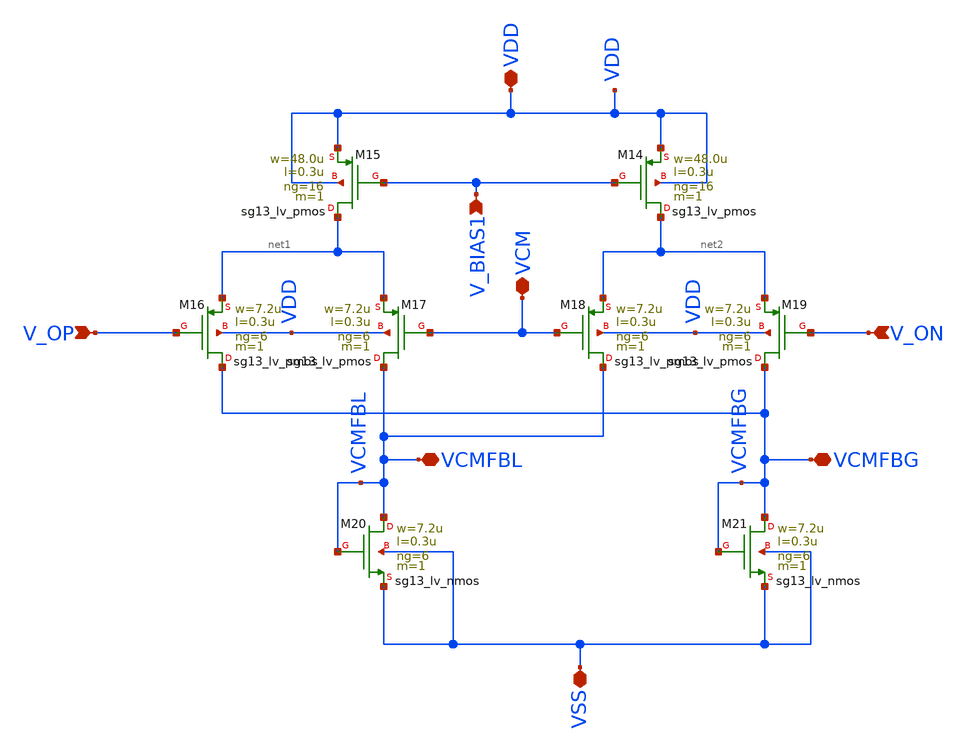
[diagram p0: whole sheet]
** sch_path: two-stage-ota-with-cmfb/Layout_PEX_PostSimulation/LAYOUT/SCHEMATIC_FOR_LAYOUT/CMFB_Block/CMFB_Block.sch
**.subckt CMFB_Block V_OP V_ON V_BIAS1 VCMFBL VCMFBG VSS VDD VCM
*.ipin V_OP
*.ipin V_ON
*.ipin V_BIAS1
*.iopin VCMFBL
*.iopin VCMFBG
*.iopin VSS
*.iopin VDD
*.iopin VCM
XM14 net2 V_BIAS1 VDD VDD sg13_lv_pmos w=48.0u l=0.3u ng=16 m=1 mm_ok=1
XM15 net1 V_BIAS1 VDD VDD sg13_lv_pmos w=48.0u l=0.3u ng=16 m=1 mm_ok=1
XM16 VCMFBG V_OP net1 VDD sg13_lv_pmos w=7.2u l=0.3u ng=6 m=1 mm_ok=1
XM17 VCMFBL VCM net1 VDD sg13_lv_pmos w=7.2u l=0.3u ng=6 m=1 mm_ok=1
XM18 VCMFBL VCM net2 VDD sg13_lv_pmos w=7.2u l=0.3u ng=6 m=1 mm_ok=1
XM19 VCMFBG V_ON net2 VDD sg13_lv_pmos w=7.2u l=0.3u ng=6 m=1 mm_ok=1
XM20 VCMFBL VCMFBL VSS VSS sg13_lv_nmos w=7.2u l=0.3u ng=6 m=1 mm_ok=1
XM21 VCMFBG VCMFBG VSS VSS sg13_lv_nmos w=7.2u l=0.3u ng=6 m=1 mm_ok=1
**.ends
.end
